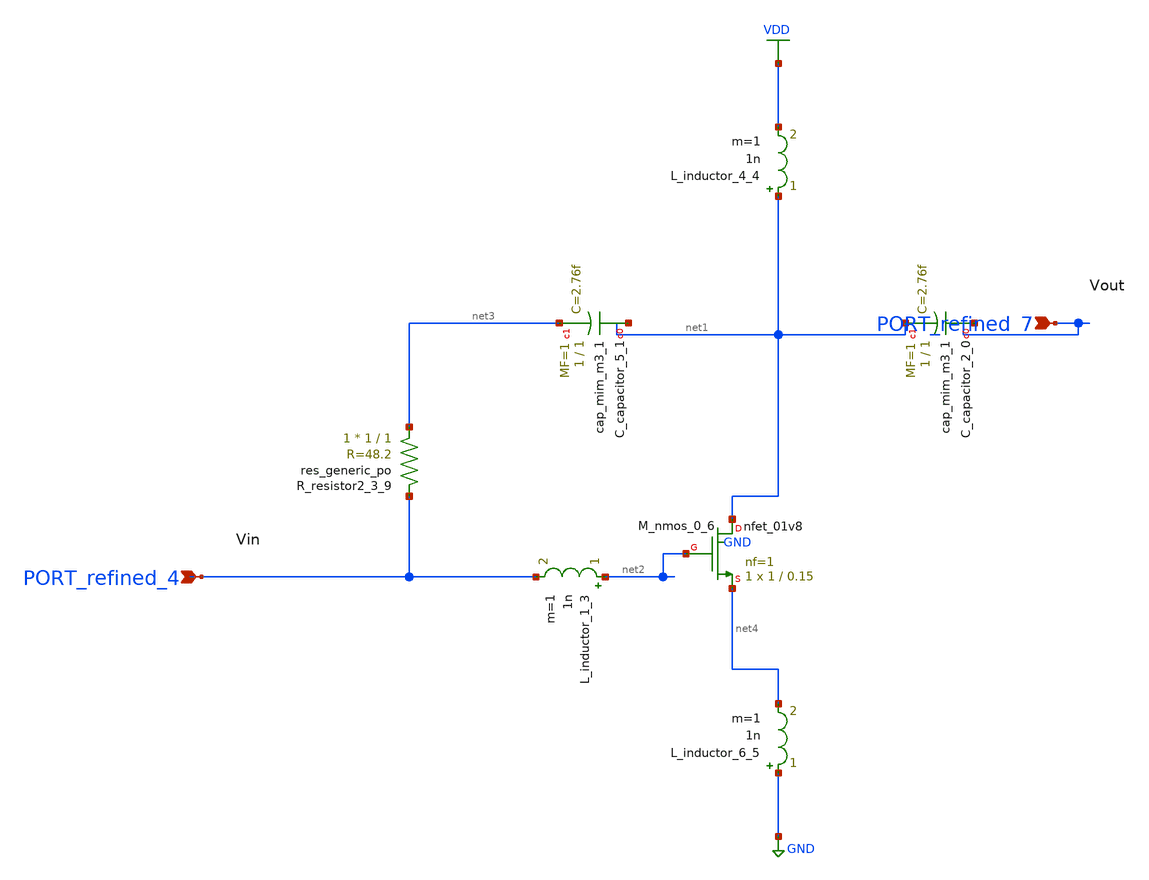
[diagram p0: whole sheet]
** sch_path: schematics/no_doi_42_002.sch
**.subckt no_doi_42_002 PORT_refined_7 PORT_refined_4
*.ipin PORT_refined_7
*.ipin PORT_refined_4
XC_capacitor_2_0 PORT_refined_7 net1 sky130_fd_pr__cap_mim_m3_1 W=1 L=1 MF=1 m=1
XC_capacitor_5_1 net1 net3 sky130_fd_pr__cap_mim_m3_1 W=1 L=1 MF=1 m=1
L_inductor_1_3 net2 PORT_refined_4 1n m=1
L_inductor_4_4 net1 VDD 1n m=1
L_inductor_6_5 GND net4 1n m=1
XM_nmos_0_6 net1 net2 net4 GND sky130_fd_pr__nfet_01v8 L=0.15 W=1 nf=1 ad='int((1 + 1)/2) * 1 / 1 * 0.29'
+ as='int((1 + 2)/2) * 1 / 1 * 0.29' pd='2*int((1 + 1)/2) * (1 / 1 + 0.29)' ps='2*int((1 + 2)/2) * (1 / 1 + 0.29)'
+ nrd='0.29 / 1 ' nrs='0.29 / 1 ' sa=0 sb=0 sd=0 mult=1 m=1
XR_resistor2_3_9 net3 PORT_refined_4 sky130_fd_pr__res_generic_po W=1 L=1 m=1
**.ends
.GLOBAL GND
.GLOBAL VDD
.end
